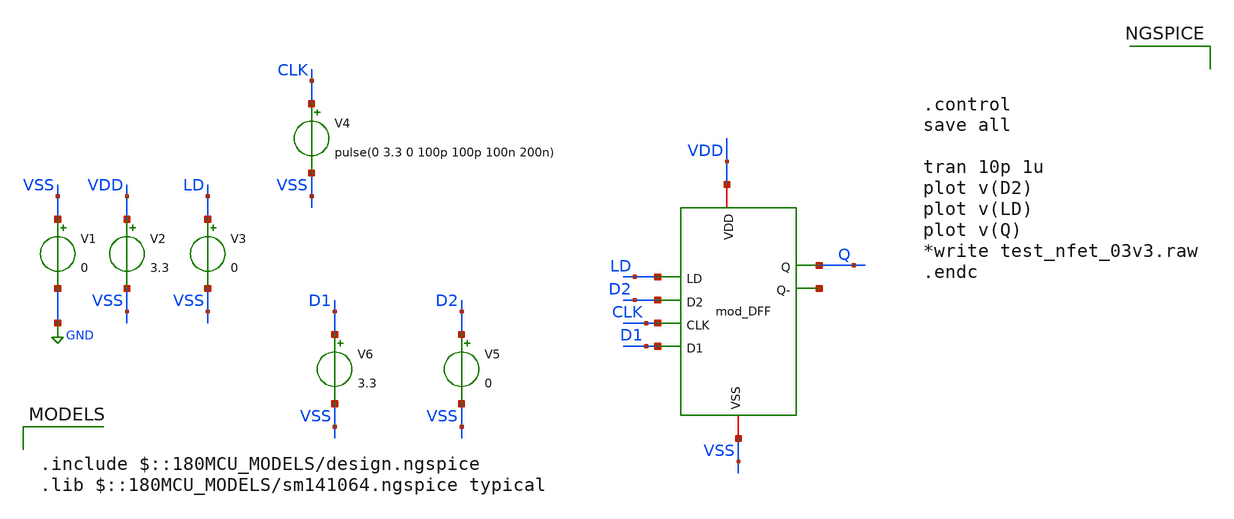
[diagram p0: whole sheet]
** sch_path: Clock_Generator_PAKISTAN_06/Schematics/mod_DFF_tb.sch
**.subckt mod_DFF_tb
x1 VDD LD D2 VSS CLK Q D1 net1 mod_DFF
V1 VSS GND 0
V2 VDD VSS 3.3
V3 LD VSS 0
V4 CLK VSS pulse(0 3.3 0 100p 100p 100n 200n)
V5 D2 VSS 0
V6 D1 VSS 3.3
**** begin user architecture code

.include $::180MCU_MODELS/design.ngspice
.lib $::180MCU_MODELS/sm141064.ngspice typical




.control
save all

tran 10p 1u
plot v(D2)
plot v(LD)
plot v(Q)
*write test_nfet_03v3.raw
.endc


**** end user architecture code
**.ends
.GLOBAL GND
.end
